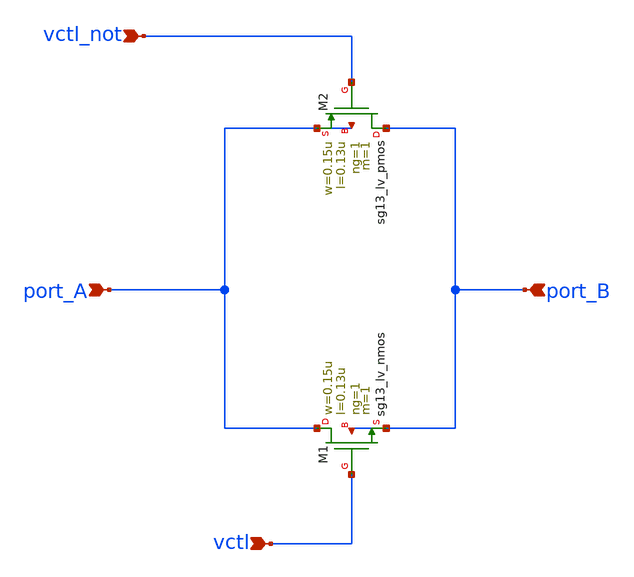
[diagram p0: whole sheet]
** sch_path: analog-db/templates/transmission_gate/transmission_gate_pair_body_tied.sch
* Copyright 2026 MacAnalog Research Group
**.subckt transmission_gate_pair_body_tied port_A port_B vctl vctl_not
*.ipin port_A
*.ipin port_B
*.ipin vctl
*.ipin vctl_not
XM1 port_A vctl port_B port_B sg13_lv_nmos w=0.15u l=0.13u ng=1 m=1 mm_ok=1
XM2 port_B vctl_not port_A port_A sg13_lv_pmos w=0.15u l=0.13u ng=1 m=1 mm_ok=1
**.ends
.end
